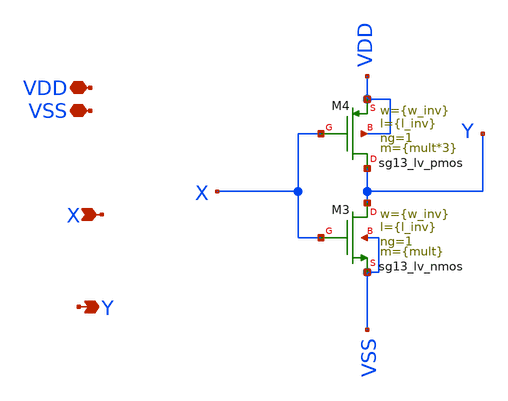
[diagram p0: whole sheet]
** sch_path: xschem/DigitalGates/INV.sch
**.subckt INV VDD X Y VSS
*.iopin VDD
*.ipin X
*.opin Y
*.iopin VSS
XM3 Y X VSS VSS sg13_lv_nmos w={w_inv} l={l_inv} ng=1 m={mult} mm_ok=1
XM4 Y X VDD VDD sg13_lv_pmos w={w_inv} l={l_inv} ng=1 m={mult*3} mm_ok=1
**** begin user architecture code



**** end user architecture code
**.ends
.end
